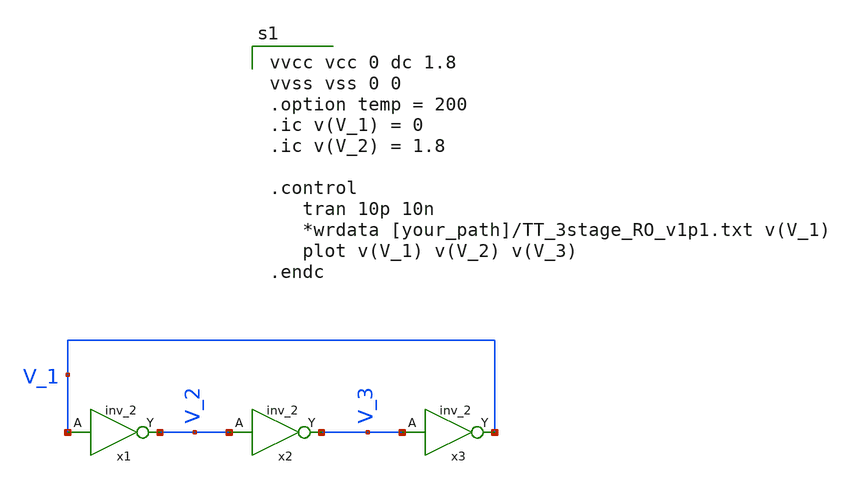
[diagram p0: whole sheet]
** sch_path: tb_3stage_RO_UNIC-CASS2024.sch
.lib $::SKYWATER_MODELS/sky130.lib.spice tt
.include $::SKYWATER_STDCELLS/sky130_fd_sc_hd.spice

**.subckt tb_3stage_RO_UNIC-CASS2024
x1 V_1 VSS VSS VCC VCC V_2 sky130_fd_sc_hd__inv_2
x2 V_2 VSS VSS VCC VCC V_3 sky130_fd_sc_hd__inv_2
x3 V_3 VSS VSS VCC VCC V_1 sky130_fd_sc_hd__inv_2
**** begin user architecture code

vvcc vcc 0 dc 1.8
vvss vss 0 0
.option temp = 200
.ic v(V_1) = 0
.ic v(V_2) = 1.8

.control
   tran 10p 10n
   *wrdata [your_path]/TT_3stage_RO_v1p1.txt v(V_1)
   plot v(V_1) v(V_2) v(V_3)
.endc


**** end user architecture code
**.ends
.end
